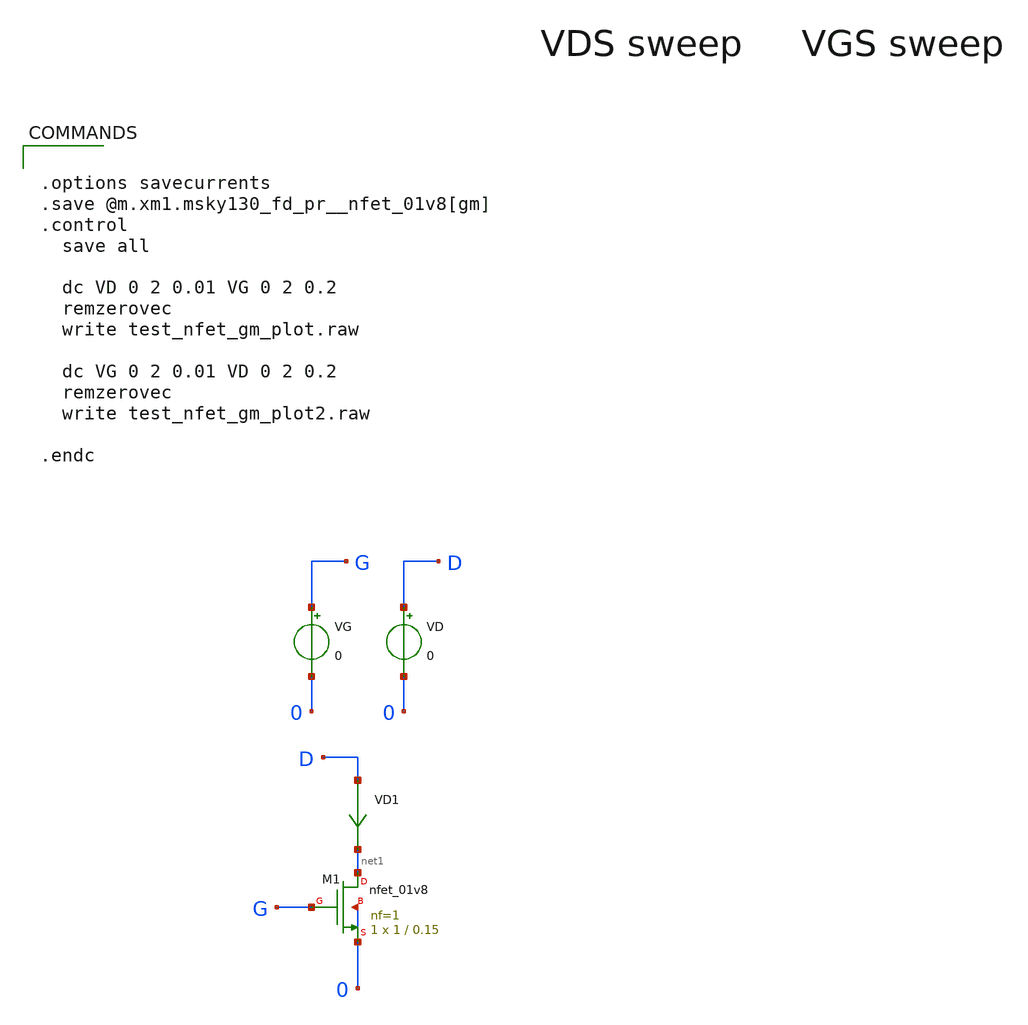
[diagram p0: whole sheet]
** sch_path: strongARM/test_nfet_gm_plot.sch
**.subckt test_nfet_gm_plot
XM1 net1 G 0 0 sky130_fd_pr__nfet_01v8 L=0.15 W=1 nf=1 ad='int((nf+1)/2) * W/nf * 0.29' as='int((nf+2)/2) * W/nf * 0.29'
+ pd='2*int((nf+1)/2) * (W/nf + 0.29)' ps='2*int((nf+2)/2) * (W/nf + 0.29)' nrd='0.29 / W' nrs='0.29 / W'
+ sa=0 sb=0 sd=0 mult=1 m=1
VG G 0 0
VD D 0 0
VD1 D net1 0
.save i(vd1)
**** begin user architecture code


.options savecurrents
.save @m.xm1.msky130_fd_pr__nfet_01v8[gm]
.control
  save all

  dc VD 0 2 0.01 VG 0 2 0.2
  remzerovec
  write test_nfet_gm_plot.raw

  dc VG 0 2 0.01 VD 0 2 0.2
  remzerovec
  write test_nfet_gm_plot2.raw

.endc



** opencircuitdesign pdks install
.lib $::SKYWATER_MODELS/sky130.lib.spice tt


**** end user architecture code
**.ends
.end
